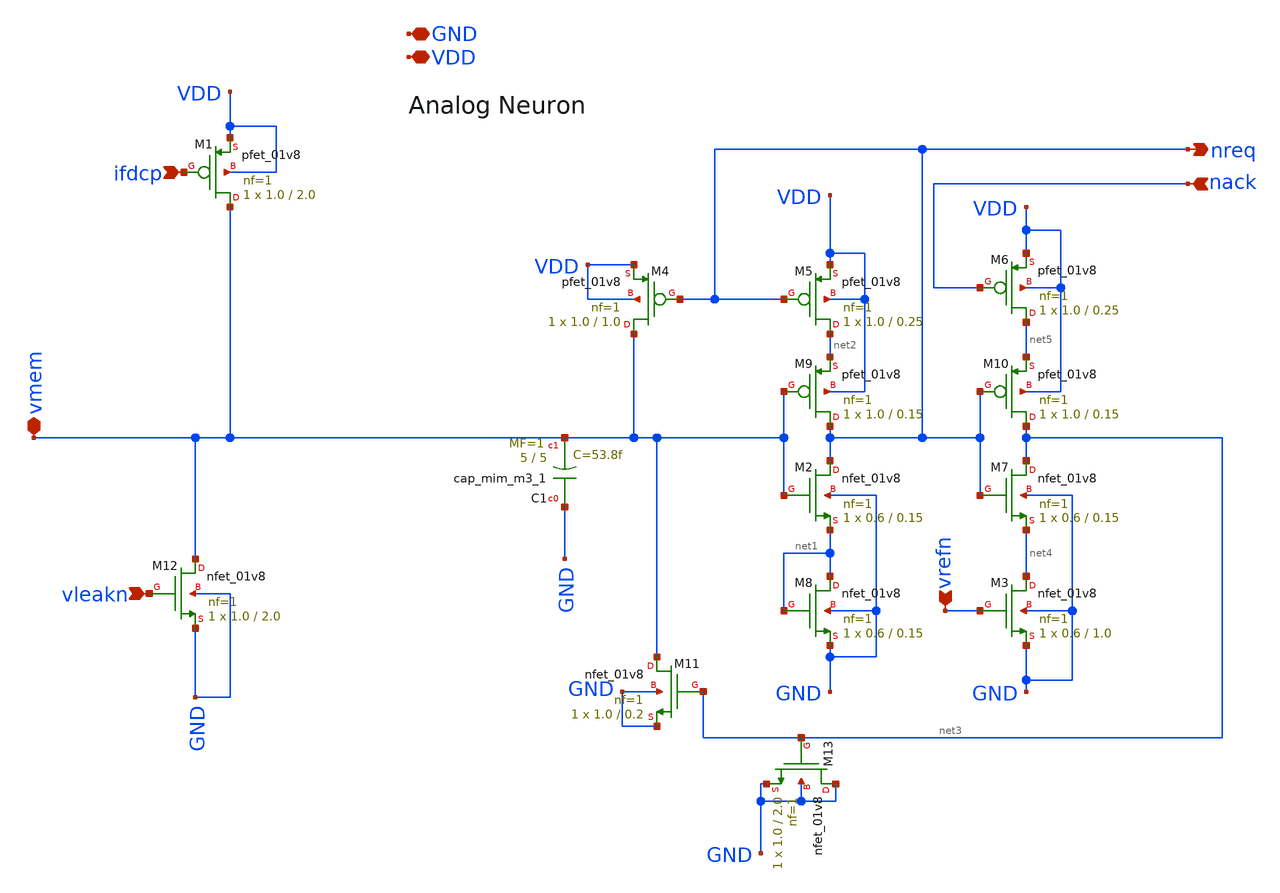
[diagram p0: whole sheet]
** sch_path: design/xschem/neuron_analog_fc_v2_norail.sch
**.subckt neuron_analog_fc_v2_norail vleakn GND VDD nreq vrefn nack ifdcp vmem
*.ipin vleakn
*.iopin GND
*.iopin VDD
*.opin nreq
*.ipin vrefn
*.ipin nack
*.ipin ifdcp
*.iopin vmem
XC1 GND vmem sky130_fd_pr__cap_mim_m3_1 W=5 L=5 MF=1 m=1
XM1 vmem ifdcp VDD VDD sky130_fd_pr__pfet_01v8 L=2.0 W=1.0 nf=1 ad='int((nf+1)/2) * W/nf * 0.29' as='int((nf+2)/2) * W/nf * 0.29'
+ pd='2*int((nf+1)/2) * (W/nf + 0.29)' ps='2*int((nf+2)/2) * (W/nf + 0.29)' nrd='0.29 / W' nrs='0.29 / W'
+ sa=0 sb=0 sd=0 mult=1 m=1
XM5 net2 nreq VDD VDD sky130_fd_pr__pfet_01v8 L=0.25 W=1.0 nf=1 ad='int((nf+1)/2) * W/nf * 0.29' as='int((nf+2)/2) * W/nf * 0.29'
+ pd='2*int((nf+1)/2) * (W/nf + 0.29)' ps='2*int((nf+2)/2) * (W/nf + 0.29)' nrd='0.29 / W' nrs='0.29 / W'
+ sa=0 sb=0 sd=0 mult=1 m=1
XM7 net3 nreq net4 GND sky130_fd_pr__nfet_01v8 L=0.15 W=0.6 nf=1 ad='int((nf+1)/2) * W/nf * 0.29' as='int((nf+2)/2) * W/nf * 0.29'
+ pd='2*int((nf+1)/2) * (W/nf + 0.29)' ps='2*int((nf+2)/2) * (W/nf + 0.29)' nrd='0.29 / W' nrs='0.29 / W'
+ sa=0 sb=0 sd=0 mult=1 m=1
XM6 net5 nack VDD VDD sky130_fd_pr__pfet_01v8 L=0.25 W=1.0 nf=1 ad='int((nf+1)/2) * W/nf * 0.29' as='int((nf+2)/2) * W/nf * 0.29'
+ pd='2*int((nf+1)/2) * (W/nf + 0.29)' ps='2*int((nf+2)/2) * (W/nf + 0.29)' nrd='0.29 / W' nrs='0.29 / W'
+ sa=0 sb=0 sd=0 mult=1 m=1
XM9 nreq vmem net2 VDD sky130_fd_pr__pfet_01v8 L=0.15 W=1.0 nf=1 ad='int((nf+1)/2) * W/nf * 0.29' as='int((nf+2)/2) * W/nf * 0.29'
+ pd='2*int((nf+1)/2) * (W/nf + 0.29)' ps='2*int((nf+2)/2) * (W/nf + 0.29)' nrd='0.29 / W' nrs='0.29 / W'
+ sa=0 sb=0 sd=0 mult=1 m=1
XM10 net3 nreq net5 VDD sky130_fd_pr__pfet_01v8 L=0.15 W=1.0 nf=1 ad='int((nf+1)/2) * W/nf * 0.29' as='int((nf+2)/2) * W/nf * 0.29'
+ pd='2*int((nf+1)/2) * (W/nf + 0.29)' ps='2*int((nf+2)/2) * (W/nf + 0.29)' nrd='0.29 / W' nrs='0.29 / W'
+ sa=0 sb=0 sd=0 mult=1 m=1
XM4 vmem nreq VDD VDD sky130_fd_pr__pfet_01v8 L=1.0 W=1.0 nf=1 ad='int((nf+1)/2) * W/nf * 0.29' as='int((nf+2)/2) * W/nf * 0.29'
+ pd='2*int((nf+1)/2) * (W/nf + 0.29)' ps='2*int((nf+2)/2) * (W/nf + 0.29)' nrd='0.29 / W' nrs='0.29 / W'
+ sa=0 sb=0 sd=0 mult=1 m=1
XM2 nreq vmem net1 GND sky130_fd_pr__nfet_01v8 L=0.15 W=0.6 nf=1 ad='int((nf+1)/2) * W/nf * 0.29' as='int((nf+2)/2) * W/nf * 0.29'
+ pd='2*int((nf+1)/2) * (W/nf + 0.29)' ps='2*int((nf+2)/2) * (W/nf + 0.29)' nrd='0.29 / W' nrs='0.29 / W'
+ sa=0 sb=0 sd=0 mult=1 m=1
XM3 net4 vrefn GND GND sky130_fd_pr__nfet_01v8 L=1.0 W=0.6 nf=1 ad='int((nf+1)/2) * W/nf * 0.29' as='int((nf+2)/2) * W/nf * 0.29'
+ pd='2*int((nf+1)/2) * (W/nf + 0.29)' ps='2*int((nf+2)/2) * (W/nf + 0.29)' nrd='0.29 / W' nrs='0.29 / W'
+ sa=0 sb=0 sd=0 mult=1 m=1
XM8 net1 net1 GND GND sky130_fd_pr__nfet_01v8 L=0.15 W=0.6 nf=1 ad='int((nf+1)/2) * W/nf * 0.29' as='int((nf+2)/2) * W/nf * 0.29'
+ pd='2*int((nf+1)/2) * (W/nf + 0.29)' ps='2*int((nf+2)/2) * (W/nf + 0.29)' nrd='0.29 / W' nrs='0.29 / W'
+ sa=0 sb=0 sd=0 mult=1 m=1
XM11 vmem net3 GND GND sky130_fd_pr__nfet_01v8 L=0.2 W=1.0 nf=1 ad='int((nf+1)/2) * W/nf * 0.29' as='int((nf+2)/2) * W/nf * 0.29'
+ pd='2*int((nf+1)/2) * (W/nf + 0.29)' ps='2*int((nf+2)/2) * (W/nf + 0.29)' nrd='0.29 / W' nrs='0.29 / W'
+ sa=0 sb=0 sd=0 mult=1 m=1
XM12 vmem vleakn GND GND sky130_fd_pr__nfet_01v8 L=2.0 W=1.0 nf=1 ad='int((nf+1)/2) * W/nf * 0.29' as='int((nf+2)/2) * W/nf * 0.29'
+ pd='2*int((nf+1)/2) * (W/nf + 0.29)' ps='2*int((nf+2)/2) * (W/nf + 0.29)' nrd='0.29 / W' nrs='0.29 / W'
+ sa=0 sb=0 sd=0 mult=1 m=1
XM13 GND net3 GND GND sky130_fd_pr__nfet_01v8 L=2.0 W=1.0 nf=1 ad='int((nf+1)/2) * W/nf * 0.29' as='int((nf+2)/2) * W/nf * 0.29'
+ pd='2*int((nf+1)/2) * (W/nf + 0.29)' ps='2*int((nf+2)/2) * (W/nf + 0.29)' nrd='0.29 / W' nrs='0.29 / W'
+ sa=0 sb=0 sd=0 mult=1 m=1
**.ends
.end
